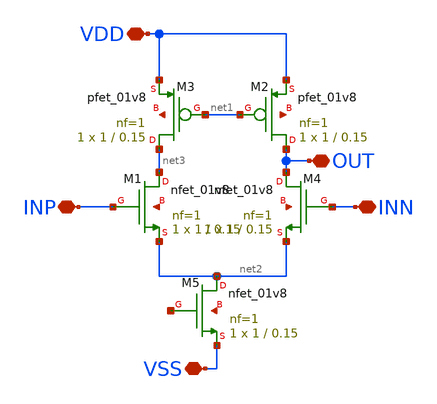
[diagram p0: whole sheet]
** sch_path: OpAmps/5TOpamp/5TOpAmp.sch
**.subckt 5TOpAmp INP VDD VSS OUT INN
*.iopin INP
*.iopin VDD
*.iopin VSS
*.iopin OUT
*.iopin INN
XM1 net3 INP net2 net4 sky130_fd_pr__nfet_01v8 L=0.15 W=1 nf=1 ad='int((nf+1)/2) * W/nf * 0.29' as='int((nf+2)/2) * W/nf * 0.29'
+ pd='2*int((nf+1)/2) * (W/nf + 0.29)' ps='2*int((nf+2)/2) * (W/nf + 0.29)' nrd='0.29 / W' nrs='0.29 / W'
+ sa=0 sb=0 sd=0 mult=1 m=1
XM2 OUT net1 VDD net5 sky130_fd_pr__pfet_01v8 L=0.15 W=1 nf=1 ad='int((nf+1)/2) * W/nf * 0.29' as='int((nf+2)/2) * W/nf * 0.29'
+ pd='2*int((nf+1)/2) * (W/nf + 0.29)' ps='2*int((nf+2)/2) * (W/nf + 0.29)' nrd='0.29 / W' nrs='0.29 / W'
+ sa=0 sb=0 sd=0 mult=1 m=1
XM3 net3 net1 VDD net6 sky130_fd_pr__pfet_01v8 L=0.15 W=1 nf=1 ad='int((nf+1)/2) * W/nf * 0.29' as='int((nf+2)/2) * W/nf * 0.29'
+ pd='2*int((nf+1)/2) * (W/nf + 0.29)' ps='2*int((nf+2)/2) * (W/nf + 0.29)' nrd='0.29 / W' nrs='0.29 / W'
+ sa=0 sb=0 sd=0 mult=1 m=1
XM4 OUT INN net2 net7 sky130_fd_pr__nfet_01v8 L=0.15 W=1 nf=1 ad='int((nf+1)/2) * W/nf * 0.29' as='int((nf+2)/2) * W/nf * 0.29'
+ pd='2*int((nf+1)/2) * (W/nf + 0.29)' ps='2*int((nf+2)/2) * (W/nf + 0.29)' nrd='0.29 / W' nrs='0.29 / W'
+ sa=0 sb=0 sd=0 mult=1 m=1
XM5 net2 net8 VSS net9 sky130_fd_pr__nfet_01v8 L=0.15 W=1 nf=1 ad='int((nf+1)/2) * W/nf * 0.29' as='int((nf+2)/2) * W/nf * 0.29'
+ pd='2*int((nf+1)/2) * (W/nf + 0.29)' ps='2*int((nf+2)/2) * (W/nf + 0.29)' nrd='0.29 / W' nrs='0.29 / W'
+ sa=0 sb=0 sd=0 mult=1 m=1
**** begin user architecture code


.lib /foss/pdks/sky130A/libs.tech/ngspice/sky130.lib.spice tt



**** end user architecture code
**.ends
.end
